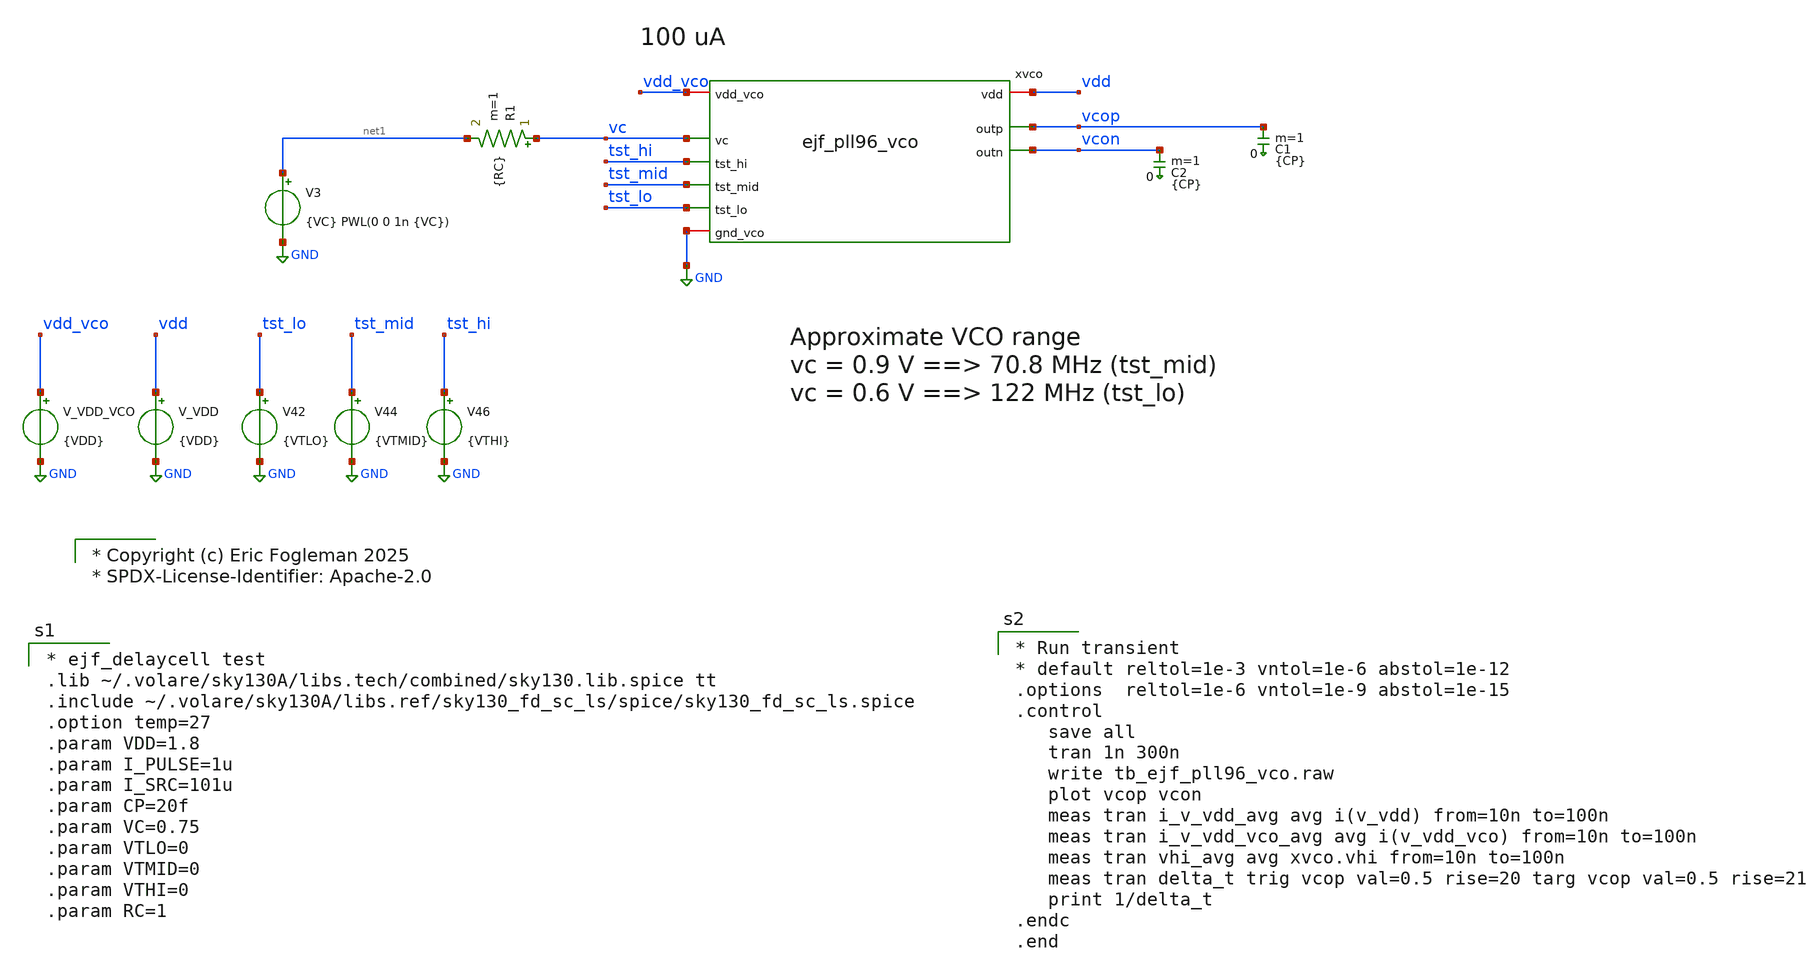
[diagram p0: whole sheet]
** sch_path: xschem/tb_ejf_pll96_vco.sch

* Copyright (c) Eric Fogleman 2025
* SPDX-License-Identifier: Apache-2.0

**.subckt tb_ejf_pll96_vco
V_VDD vdd GND {VDD}
C1 vcop 0 {CP} m=1
C2 vcon 0 {CP} m=1
V3 net1 GND {VC} PWL(0 0 1n {VC})
xvco vdd_vco vc vdd vcop vcon GND tst_hi tst_mid tst_lo ejf_pll96_vco
V_VDD_VCO vdd_vco GND {VDD}
V42 tst_lo GND {VTLO}
V44 tst_mid GND {VTMID}
V46 tst_hi GND {VTHI}
R1 vc net1 {RC} m=1
**** begin user architecture code

* ejf_delaycell test
.lib ~/.volare/sky130A/libs.tech/combined/sky130.lib.spice tt
.include ~/.volare/sky130A/libs.ref/sky130_fd_sc_ls/spice/sky130_fd_sc_ls.spice
.option temp=27
.param VDD=1.8
.param I_PULSE=1u
.param I_SRC=101u
.param CP=20f
.param VC=0.75
.param VTLO=0
.param VTMID=0
.param VTHI=0
.param RC=1



* Run transient
* default reltol=1e-3 vntol=1e-6 abstol=1e-12
.options  reltol=1e-6 vntol=1e-9 abstol=1e-15
.control
   save all
   tran 1n 300n
   write tb_ejf_pll96_vco.raw
   plot vcop vcon
   meas tran i_v_vdd_avg avg i(v_vdd) from=10n to=100n
   meas tran i_v_vdd_vco_avg avg i(v_vdd_vco) from=10n to=100n
   meas tran vhi_avg avg xvco.vhi from=10n to=100n
   meas tran delta_t trig vcop val=0.5 rise=20 targ vcop val=0.5 rise=21
   print 1/delta_t
.endc
.end

**** end user architecture code
**.ends
.GLOBAL GND
.end
